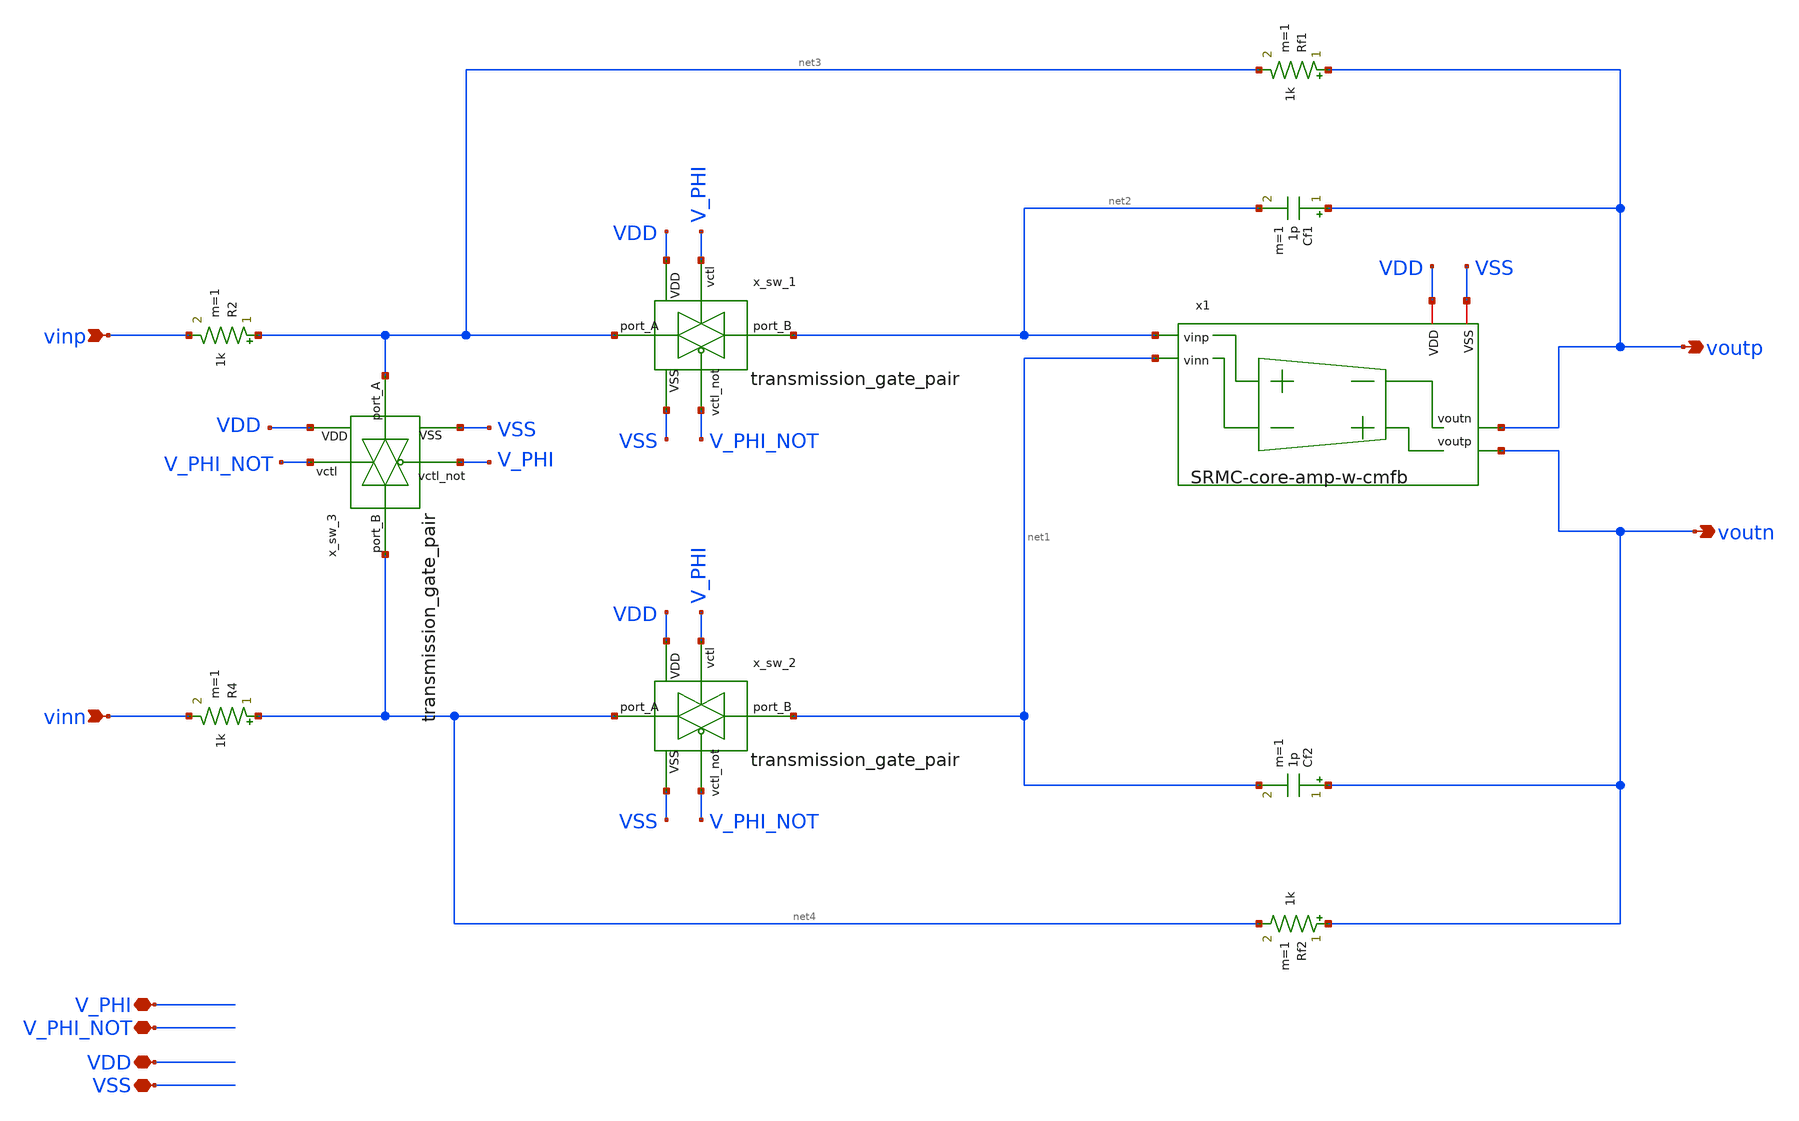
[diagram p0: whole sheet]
** sch_path: analog-db/drawings/bio-afe-01-YuPinHsu-reconfigable-SRMC/SRMC.sch
* Copyright 2026 MacAnalog Research Group
**.subckt SRMC V_PHI V_PHI_NOT vinp vinn voutn voutp VDD VSS
*.iopin V_PHI
*.iopin V_PHI_NOT
*.ipin vinp
*.ipin vinn
*.opin voutn
*.opin voutp
*.iopin VDD
*.iopin VSS
Rf1 voutp net3 1k m=1
Cf1 voutp net2 1p m=1
Rf2 voutn net4 1k m=1
Cf2 voutn net1 1p m=1
R2 net3 vinp 1k m=1
R4 net4 vinn 1k m=1
x1 net2 net1 voutn voutp VDD VSS SRMC-core-amp-w-cmfb
x_sw_1 V_PHI_NOT VDD net2 VSS net3 V_PHI transmission_gate_pair
x_sw_2 V_PHI_NOT VDD net1 VSS net4 V_PHI transmission_gate_pair
x_sw_3 V_PHI VDD net4 VSS net3 V_PHI_NOT transmission_gate_pair
**.ends
.end
